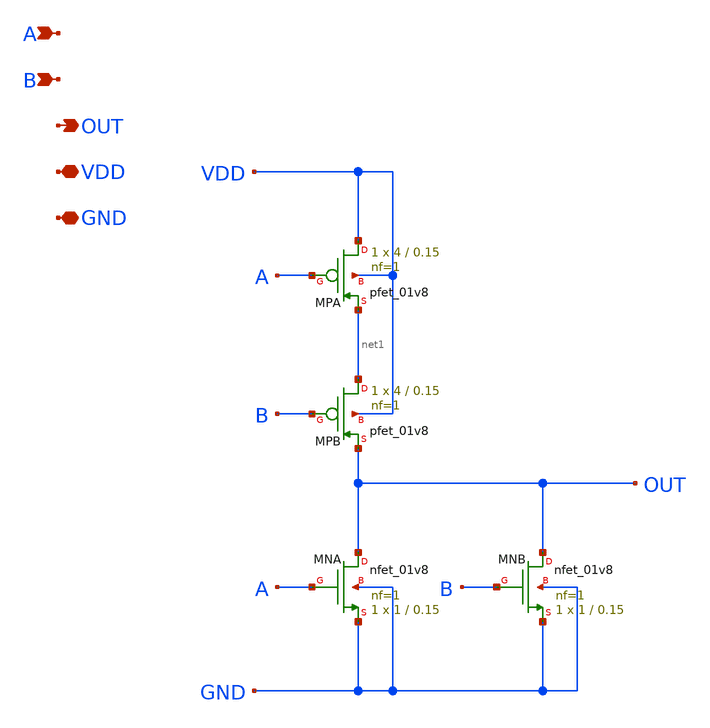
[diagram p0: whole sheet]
** sch_path: blocks/06_Clock_gen/xschem/B6_NOR2.sch
**.subckt B6_NOR2 A B OUT VDD GND
*.ipin A
*.ipin B
*.opin OUT
*.iopin VDD
*.iopin GND
XMPA VDD A net1 VDD sky130_fd_pr__pfet_01v8 L=0.15 W=4 nf=1 ad='int((1 + 1)/2) * 4 / 1 * 0.29' as='int((1 + 2)/2) * 4 / 1 * 0.29'
+ pd='2*int((1 + 1)/2) * (4 / 1 + 0.29)' ps='2*int((1 + 2)/2) * (4 / 1 + 0.29)' nrd='0.29 / 4 ' nrs='0.29 / 4 '
+ sa=0 sb=0 sd=0 mult=1 m=1
XMPB net1 B OUT VDD sky130_fd_pr__pfet_01v8 L=0.15 W=4 nf=1 ad='int((1 + 1)/2) * 4 / 1 * 0.29' as='int((1 + 2)/2) * 4 / 1 * 0.29'
+ pd='2*int((1 + 1)/2) * (4 / 1 + 0.29)' ps='2*int((1 + 2)/2) * (4 / 1 + 0.29)' nrd='0.29 / 4 ' nrs='0.29 / 4 '
+ sa=0 sb=0 sd=0 mult=1 m=1
XMNA OUT A GND GND sky130_fd_pr__nfet_01v8 L=0.15 W=1 nf=1 ad='int((1 + 1)/2) * 1 / 1 * 0.29' as='int((1 + 2)/2) * 1 / 1 * 0.29'
+ pd='2*int((1 + 1)/2) * (1 / 1 + 0.29)' ps='2*int((1 + 2)/2) * (1 / 1 + 0.29)' nrd='0.29 / 1 ' nrs='0.29 / 1 '
+ sa=0 sb=0 sd=0 mult=1 m=1
XMNB OUT B GND GND sky130_fd_pr__nfet_01v8 L=0.15 W=1 nf=1 ad='int((1 + 1)/2) * 1 / 1 * 0.29' as='int((1 + 2)/2) * 1 / 1 * 0.29'
+ pd='2*int((1 + 1)/2) * (1 / 1 + 0.29)' ps='2*int((1 + 2)/2) * (1 / 1 + 0.29)' nrd='0.29 / 1 ' nrs='0.29 / 1 '
+ sa=0 sb=0 sd=0 mult=1 m=1
**.ends
.end
